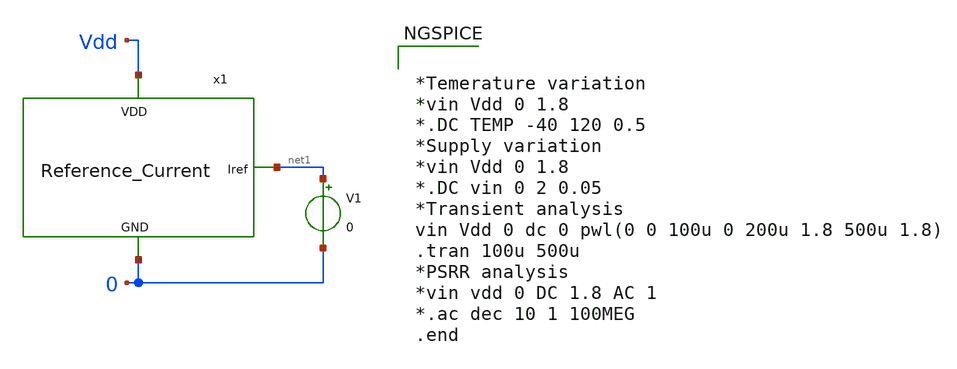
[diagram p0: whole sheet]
** sch_path: Analog_Blocks/Reference_Current/Schematic/Reference_Current_TB.sch
**.subckt Reference_Current_TB
V1 net1 0 0
x1 Vdd net1 0 Reference_Current
**** begin user architecture code


*Temerature variation
*vin Vdd 0 1.8
*.DC TEMP -40 120 0.5
*Supply variation
*vin Vdd 0 1.8
*.DC vin 0 2 0.05
*Transient analysis
vin Vdd 0 dc 0 pwl(0 0 100u 0 200u 1.8 500u 1.8)
.tran 100u 500u
*PSRR analysis
*vin vdd 0 DC 1.8 AC 1
*.ac dec 10 1 100MEG
.end



.include $::SKYWATER_MODELS/cells/nfet_01v8/sky130_fd_pr__nfet_01v8__tt.corner.spice
.include $::SKYWATER_MODELS/cells/nfet_01v8_lvt/sky130_fd_pr__nfet_01v8_lvt__tt.corner.spice
.include $::SKYWATER_MODELS/cells/pfet_01v8/sky130_fd_pr__pfet_01v8__tt.corner.spice
.include $::SKYWATER_MODELS/cells/nfet_03v3_nvt/sky130_fd_pr__nfet_03v3_nvt__tt.corner.spice
.include $::SKYWATER_MODELS/cells/nfet_05v0_nvt/sky130_fd_pr__nfet_05v0_nvt__tt.corner.spice
.include $::SKYWATER_MODELS/cells/esd_nfet_01v8/sky130_fd_pr__esd_nfet_01v8__tt.corner.spice
.include $::SKYWATER_MODELS/cells/pfet_01v8_lvt/sky130_fd_pr__pfet_01v8_lvt__tt.corner.spice
.include $::SKYWATER_MODELS/cells/pfet_01v8_hvt/sky130_fd_pr__pfet_01v8_hvt__tt.corner.spice
.include $::SKYWATER_MODELS/cells/esd_pfet_g5v0d10v5/sky130_fd_pr__esd_pfet_g5v0d10v5__tt.corner.spice
.include $::SKYWATER_MODELS/cells/pfet_g5v0d10v5/sky130_fd_pr__pfet_g5v0d10v5__tt.corner.spice
.include $::SKYWATER_MODELS/cells/pfet_g5v0d16v0/sky130_fd_pr__pfet_g5v0d16v0__tt.corner.spice
.include $::SKYWATER_MODELS/cells/nfet_g5v0d10v5/sky130_fd_pr__nfet_g5v0d10v5__tt.corner.spice
.include $::SKYWATER_MODELS/cells/nfet_g5v0d16v0/sky130_fd_pr__nfet_g5v0d16v0__tt_discrete.corner.spice
.include $::SKYWATER_MODELS/cells/esd_nfet_g5v0d10v5/sky130_fd_pr__esd_nfet_g5v0d10v5__tt.corner.spice
.include $::SKYWATER_MODELS/models/corners/tt/nonfet.spice
* Mismatch parameters
.include $::SKYWATER_MODELS/cells/nfet_01v8/sky130_fd_pr__nfet_01v8__mismatch.corner.spice
.include $::SKYWATER_MODELS/cells/pfet_01v8/sky130_fd_pr__pfet_01v8__mismatch.corner.spice
.include $::SKYWATER_MODELS/cells/nfet_01v8_lvt/sky130_fd_pr__nfet_01v8_lvt__mismatch.corner.spice
.include $::SKYWATER_MODELS/cells/pfet_01v8_lvt/sky130_fd_pr__pfet_01v8_lvt__mismatch.corner.spice
.include $::SKYWATER_MODELS/cells/pfet_01v8_hvt/sky130_fd_pr__pfet_01v8_hvt__mismatch.corner.spice
.include $::SKYWATER_MODELS/cells/nfet_g5v0d10v5/sky130_fd_pr__nfet_g5v0d10v5__mismatch.corner.spice
.include $::SKYWATER_MODELS/cells/pfet_g5v0d10v5/sky130_fd_pr__pfet_g5v0d10v5__mismatch.corner.spice
.include $::SKYWATER_MODELS/cells/nfet_05v0_nvt/sky130_fd_pr__nfet_05v0_nvt__mismatch.corner.spice
.include $::SKYWATER_MODELS/cells/nfet_03v3_nvt/sky130_fd_pr__nfet_03v3_nvt__mismatch.corner.spice
* Resistor$::SKYWATER_MODELS/Capacitor
.include $::SKYWATER_MODELS/models/r+c/res_typical__cap_typical.spice
.include $::SKYWATER_MODELS/models/r+c/res_typical__cap_typical__lin.spice
* Special cells
.include $::SKYWATER_MODELS/models/corners/tt/specialized_cells.spice
* All models
.include $::SKYWATER_MODELS/models/all.spice
* Corner
.include $::SKYWATER_MODELS/models/corners/tt/rf.spice

**** end user architecture code
**.ends

* expanding   symbol:  /home/eslam/Analog_Design/Reference_Current/Schematic/Reference_Current.sym #
*+ of pins=3
** sym_path: Analog_Blocks/Reference_Current/Schematic/Reference_Current.sym
** sch_path: Analog_Blocks/Reference_Current/Schematic/Reference_Current.sch
.subckt Reference_Current VDD Iref GND
*.ipin VDD
*.ipin GND
*.opin Iref
R1 net3 net5 7k m=1
XQ1 GND GND net5 sky130_fd_pr__pnp_05v5_W0p68L0p68 m=1
XQ2 GND GND net5 sky130_fd_pr__pnp_05v5_W0p68L0p68 m=1
XQ3 GND GND net6 sky130_fd_pr__pnp_05v5_W0p68L0p68 m=1
R2 net8 GND 54k m=1
XQ6 GND GND net9 sky130_fd_pr__pnp_05v5_W0p68L0p68 m=1
XM1 net1 net2 net3 GND sky130_fd_pr__nfet_01v8_lvt L=1 W=10 nf=1 ad='int((nf+1)/2) * W/nf * 0.29' as='int((nf+2)/2) * W/nf * 0.29'
+ pd='2*int((nf+1)/2) * (W/nf + 0.29)' ps='2*int((nf+2)/2) * (W/nf + 0.29)' nrd='0.29 / W' nrs='0.29 / W'
+ sa=0 sb=0 sd=0 mult=1 m=1
XM2 net2 net2 net6 GND sky130_fd_pr__nfet_01v8_lvt L=1 W=10 nf=1 ad='int((nf+1)/2) * W/nf * 0.29' as='int((nf+2)/2) * W/nf * 0.29'
+ pd='2*int((nf+1)/2) * (W/nf + 0.29)' ps='2*int((nf+2)/2) * (W/nf + 0.29)' nrd='0.29 / W' nrs='0.29 / W'
+ sa=0 sb=0 sd=0 mult=1 m=1
XM3 net1 net1 VDD VDD sky130_fd_pr__pfet_01v8_lvt L=1 W=10 nf=1 ad='int((nf+1)/2) * W/nf * 0.29' as='int((nf+2)/2) * W/nf * 0.29'
+ pd='2*int((nf+1)/2) * (W/nf + 0.29)' ps='2*int((nf+2)/2) * (W/nf + 0.29)' nrd='0.29 / W' nrs='0.29 / W'
+ sa=0 sb=0 sd=0 mult=1 m=1
XM4 net2 net1 VDD VDD sky130_fd_pr__pfet_01v8_lvt L=1 W=10 nf=1 ad='int((nf+1)/2) * W/nf * 0.29' as='int((nf+2)/2) * W/nf * 0.29'
+ pd='2*int((nf+1)/2) * (W/nf + 0.29)' ps='2*int((nf+2)/2) * (W/nf + 0.29)' nrd='0.29 / W' nrs='0.29 / W'
+ sa=0 sb=0 sd=0 mult=1 m=1
XM5 net4 net7 net8 GND sky130_fd_pr__nfet_01v8_lvt L=1 W=10 nf=1 ad='int((nf+1)/2) * W/nf * 0.29' as='int((nf+2)/2) * W/nf * 0.29'
+ pd='2*int((nf+1)/2) * (W/nf + 0.29)' ps='2*int((nf+2)/2) * (W/nf + 0.29)' nrd='0.29 / W' nrs='0.29 / W'
+ sa=0 sb=0 sd=0 mult=1 m=1
XM6 net7 net7 net9 GND sky130_fd_pr__nfet_01v8_lvt L=1 W=10 nf=1 ad='int((nf+1)/2) * W/nf * 0.29' as='int((nf+2)/2) * W/nf * 0.29'
+ pd='2*int((nf+1)/2) * (W/nf + 0.29)' ps='2*int((nf+2)/2) * (W/nf + 0.29)' nrd='0.29 / W' nrs='0.29 / W'
+ sa=0 sb=0 sd=0 mult=1 m=1
XM7 net4 net4 VDD VDD sky130_fd_pr__pfet_01v8_lvt L=1 W=10 nf=1 ad='int((nf+1)/2) * W/nf * 0.29' as='int((nf+2)/2) * W/nf * 0.29'
+ pd='2*int((nf+1)/2) * (W/nf + 0.29)' ps='2*int((nf+2)/2) * (W/nf + 0.29)' nrd='0.29 / W' nrs='0.29 / W'
+ sa=0 sb=0 sd=0 mult=1 m=1
XM8 net7 net4 VDD VDD sky130_fd_pr__pfet_01v8_lvt L=1 W=10 nf=1 ad='int((nf+1)/2) * W/nf * 0.29' as='int((nf+2)/2) * W/nf * 0.29'
+ pd='2*int((nf+1)/2) * (W/nf + 0.29)' ps='2*int((nf+2)/2) * (W/nf + 0.29)' nrd='0.29 / W' nrs='0.29 / W'
+ sa=0 sb=0 sd=0 mult=1 m=1
XM9 Iref net4 VDD VDD sky130_fd_pr__pfet_01v8_lvt L=1 W=10 nf=1 ad='int((nf+1)/2) * W/nf * 0.29' as='int((nf+2)/2) * W/nf * 0.29'
+ pd='2*int((nf+1)/2) * (W/nf + 0.29)' ps='2*int((nf+2)/2) * (W/nf + 0.29)' nrd='0.29 / W' nrs='0.29 / W'
+ sa=0 sb=0 sd=0 mult=1 m=1
XM10 Iref net1 VDD VDD sky130_fd_pr__pfet_01v8_lvt L=1 W=10 nf=1 ad='int((nf+1)/2) * W/nf * 0.29' as='int((nf+2)/2) * W/nf * 0.29'
+ pd='2*int((nf+1)/2) * (W/nf + 0.29)' ps='2*int((nf+2)/2) * (W/nf + 0.29)' nrd='0.29 / W' nrs='0.29 / W'
+ sa=0 sb=0 sd=0 mult=1 m=1
.ends

.end
